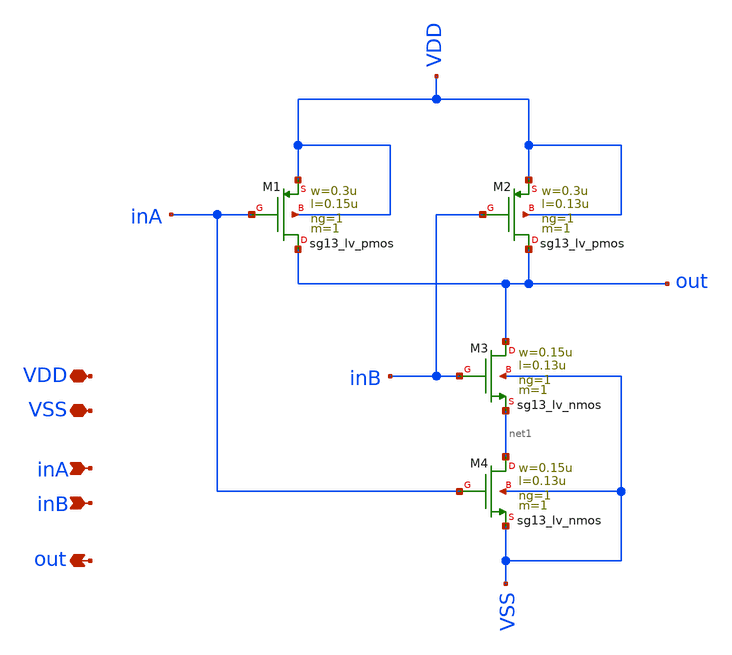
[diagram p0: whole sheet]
** sch_path: Team 2 Design/design_data/xschem/t2_nand2.sch
**.subckt t2_nand2 VSS inA inB out VDD
*.iopin VSS
*.ipin inA
*.ipin inB
*.opin out
*.iopin VDD
XM1 out inA VDD VDD sg13_lv_pmos w=0.3u l=0.15u ng=1 m=1 mm_ok=1
XM2 out inB VDD VDD sg13_lv_pmos w=0.3u l=0.13u ng=1 m=1 mm_ok=1
XM3 out inB net1 VSS sg13_lv_nmos w=0.15u l=0.13u ng=1 m=1 mm_ok=1
XM4 net1 inA VSS VSS sg13_lv_nmos w=0.15u l=0.13u ng=1 m=1 mm_ok=1
**.ends
.end
